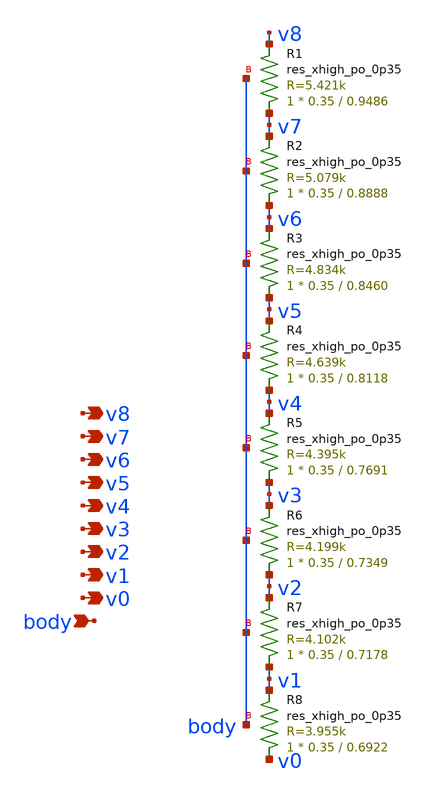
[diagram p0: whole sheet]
** sch_path: xschem/res_seg_3.sch
**.subckt res_seg_3 v8 v7 v6 v5 v4 v3 v2 v1 v0 body
*.opin v8
*.opin v7
*.opin v6
*.opin v5
*.opin v4
*.opin v3
*.opin v2
*.opin v1
*.opin v0
*.ipin body
XR1 v7 v8 body sky130_fd_pr__res_xhigh_po_0p35 L=0.9486 mult=1 m=1
XR2 v6 v7 body sky130_fd_pr__res_xhigh_po_0p35 L=0.8888 mult=1 m=1
XR3 v5 v6 body sky130_fd_pr__res_xhigh_po_0p35 L=0.8460 mult=1 m=1
XR4 v4 v5 body sky130_fd_pr__res_xhigh_po_0p35 L=0.8118 mult=1 m=1
XR5 v3 v4 body sky130_fd_pr__res_xhigh_po_0p35 L=0.7691 mult=1 m=1
XR6 v2 v3 body sky130_fd_pr__res_xhigh_po_0p35 L=0.7349 mult=1 m=1
XR7 v1 v2 body sky130_fd_pr__res_xhigh_po_0p35 L=0.7178 mult=1 m=1
XR8 v0 v1 body sky130_fd_pr__res_xhigh_po_0p35 L=0.6922 mult=1 m=1
**.ends
.end
